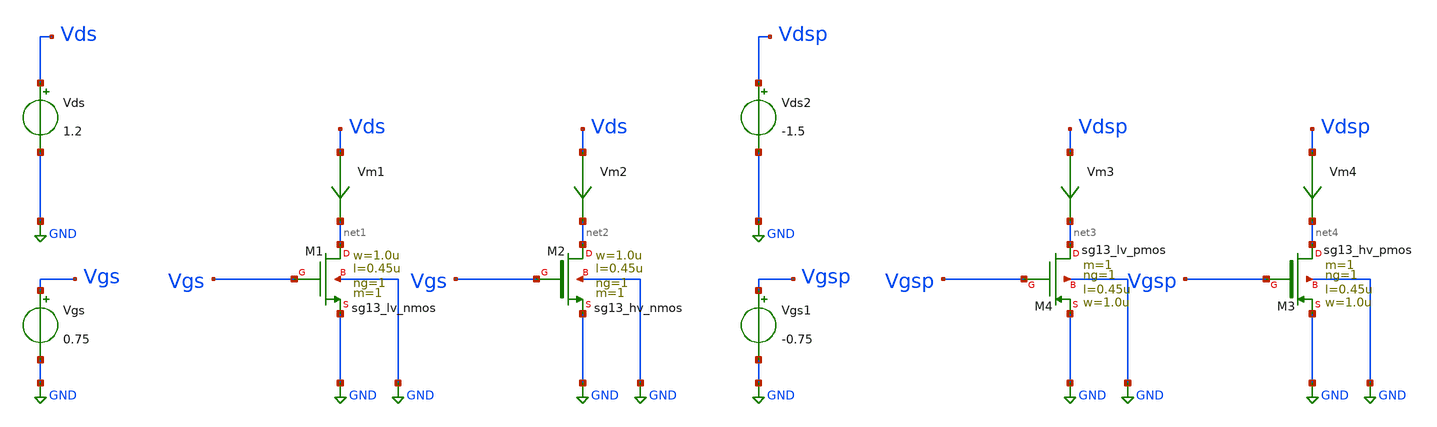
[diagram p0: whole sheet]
** sch_path: ihp-sg13g2/xschem_libs/sg13g2_tests_ase/dc_mos_temp/schematic/dc_mos_temp.sch
* Copyright 2023 IHP PDK Authors
**.subckt dc_mos_temp
Vgs Vgs GND 0.75
Vds Vds GND 1.2
Vm1 Vds net1 0
.save i(vm1)
Vm2 Vds net2 0
.save i(vm2)
Vm3 Vdsp net3 0
.save i(vm3)
Vm4 Vdsp net4 0
.save i(vm4)
Vgs1 Vgsp GND -0.75
Vds2 Vdsp GND -1.5
XM1 net1 Vgs GND GND sg13_lv_nmos w=1.0u l=0.45u ng=1 m=1 mm_ok=1
XM2 net2 Vgs GND GND sg13_hv_nmos w=1.0u l=0.45u ng=1 m=1 mm_ok=1
XM3 net4 Vgsp GND GND sg13_hv_pmos w=1.0u l=0.45u ng=1 m=1 mm_ok=1
XM4 net3 Vgsp GND GND sg13_lv_pmos w=1.0u l=0.45u ng=1 m=1 mm_ok=1
**.ends
.GLOBAL GND
.end
